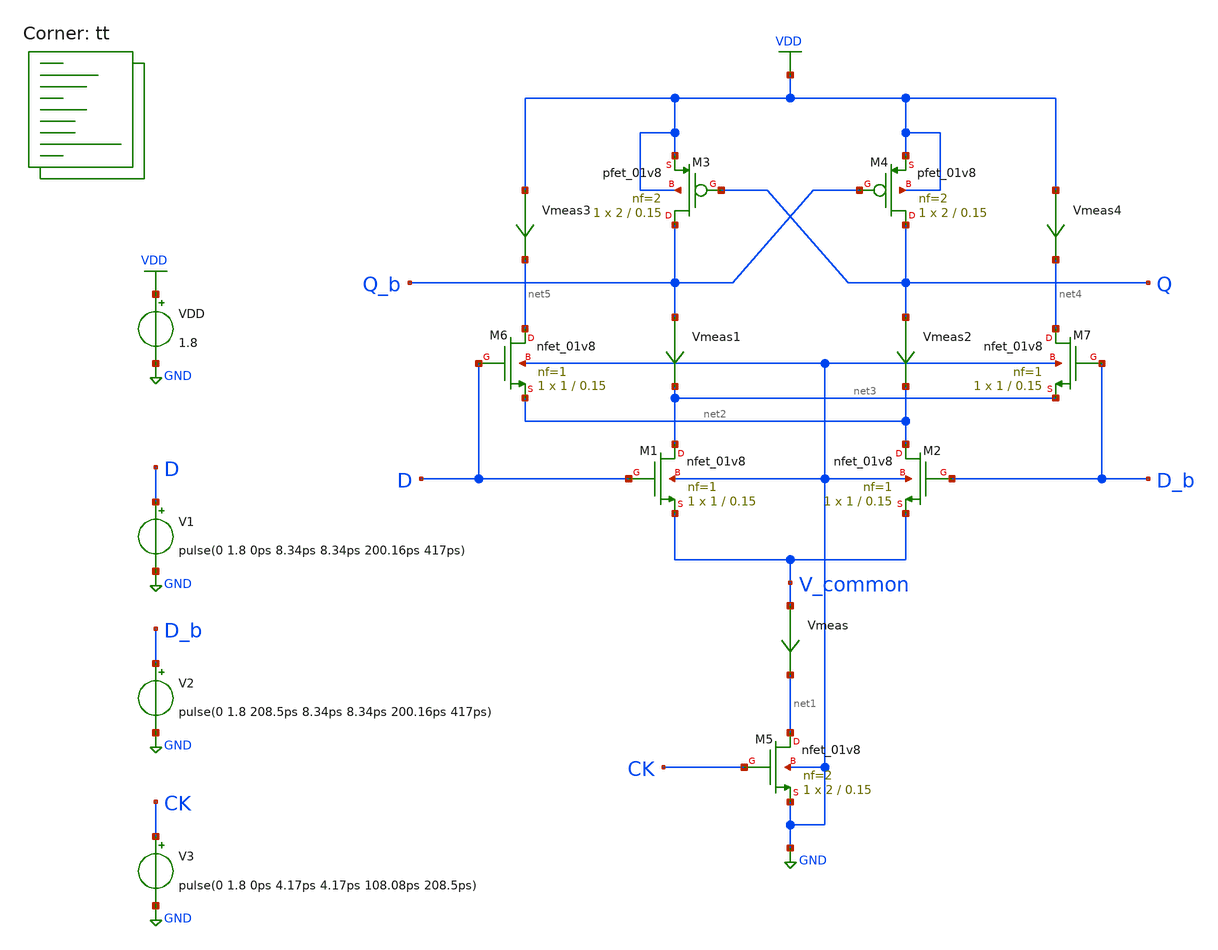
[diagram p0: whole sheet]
** sch_path: projects/pll/divider/xschem_ngspice/tb_xcp_latch_SF2.sch
**.subckt tb_xcp_latch_SF2
VDD VDD GND 1.8
V1 D GND pulse(0 1.8 0ps 8.34ps 8.34ps 200.16ps 417ps)
V2 D_b GND pulse(0 1.8 208.5ps 8.34ps 8.34ps 200.16ps 417ps)
V3 CK GND pulse(0 1.8 0ps 4.17ps 4.17ps 108.08ps 208.5ps)
XM5 net1 CK GND GND sky130_fd_pr__nfet_01v8 L=0.15 W=2 nf=2 ad='int((nf+1)/2) * W/nf * 0.29' as='int((nf+2)/2) * W/nf * 0.29'
+ pd='2*int((nf+1)/2) * (W/nf + 0.29)' ps='2*int((nf+2)/2) * (W/nf + 0.29)' nrd='0.29 / W' nrs='0.29 / W'
+ sa=0 sb=0 sd=0 mult=1 m=1
XM1 net3 D V_common GND sky130_fd_pr__nfet_01v8 L=0.15 W=1 nf=1 ad='int((nf+1)/2) * W/nf * 0.29' as='int((nf+2)/2) * W/nf * 0.29'
+ pd='2*int((nf+1)/2) * (W/nf + 0.29)' ps='2*int((nf+2)/2) * (W/nf + 0.29)' nrd='0.29 / W' nrs='0.29 / W'
+ sa=0 sb=0 sd=0 mult=1 m=1
XM2 net2 D_b V_common GND sky130_fd_pr__nfet_01v8 L=0.15 W=1 nf=1 ad='int((nf+1)/2) * W/nf * 0.29' as='int((nf+2)/2) * W/nf * 0.29'
+ pd='2*int((nf+1)/2) * (W/nf + 0.29)' ps='2*int((nf+2)/2) * (W/nf + 0.29)' nrd='0.29 / W' nrs='0.29 / W'
+ sa=0 sb=0 sd=0 mult=1 m=1
Vmeas V_common net1 0
.save i(vmeas)
Vmeas1 Q_b net3 0
.save i(vmeas1)
Vmeas2 Q net2 0
.save i(vmeas2)
XM3 Q_b Q VDD VDD sky130_fd_pr__pfet_01v8 L=0.15 W=2 nf=2 ad='int((nf+1)/2) * W/nf * 0.29' as='int((nf+2)/2) * W/nf * 0.29'
+ pd='2*int((nf+1)/2) * (W/nf + 0.29)' ps='2*int((nf+2)/2) * (W/nf + 0.29)' nrd='0.29 / W' nrs='0.29 / W'
+ sa=0 sb=0 sd=0 mult=1 m=1
XM4 Q Q_b VDD VDD sky130_fd_pr__pfet_01v8 L=0.15 W=2 nf=2 ad='int((nf+1)/2) * W/nf * 0.29' as='int((nf+2)/2) * W/nf * 0.29'
+ pd='2*int((nf+1)/2) * (W/nf + 0.29)' ps='2*int((nf+2)/2) * (W/nf + 0.29)' nrd='0.29 / W' nrs='0.29 / W'
+ sa=0 sb=0 sd=0 mult=1 m=1
XM6 net5 D net2 GND sky130_fd_pr__nfet_01v8 L=0.15 W=1 nf=1 ad='int((nf+1)/2) * W/nf * 0.29' as='int((nf+2)/2) * W/nf * 0.29'
+ pd='2*int((nf+1)/2) * (W/nf + 0.29)' ps='2*int((nf+2)/2) * (W/nf + 0.29)' nrd='0.29 / W' nrs='0.29 / W'
+ sa=0 sb=0 sd=0 mult=1 m=1
XM7 net4 D_b net3 GND sky130_fd_pr__nfet_01v8 L=0.15 W=1 nf=1 ad='int((nf+1)/2) * W/nf * 0.29' as='int((nf+2)/2) * W/nf * 0.29'
+ pd='2*int((nf+1)/2) * (W/nf + 0.29)' ps='2*int((nf+2)/2) * (W/nf + 0.29)' nrd='0.29 / W' nrs='0.29 / W'
+ sa=0 sb=0 sd=0 mult=1 m=1
Vmeas3 VDD net5 0
.save i(vmeas3)
Vmeas4 VDD net4 0
.save i(vmeas4)
**** begin user architecture code



.include /foss/pdks/sky130A/libs.ref/sky130_fd_sc_hd/spice/sky130_fd_sc_hd.spice

.option method=gear
.option wnflag=1
.option savecurrents

.save @m.xm1.msky130_fd_pr__nfet_01v8[gm] @m.xm1.msky130_fd_pr__nfet_01v8[gm] @m.xm1.msky130_fd_pr__pfet_01v8[gm] @m.xm1.msky130_fd_pr__pfet_01v8[gm] @m.xm1.msky130_fd_pr__nfet_01v8[gm] @m.xm1.msky130_fd_pr__nfet_01v8[gm] @m.xm1.msky130_fd_pr__nfet_01v8[gm] @vmeas @vmeas1 @vmeas2

*.ic v(q_b)=1.8

.control

  save v(d) v(d_b) v(q) v(q_b) v(q1) v(q1_b) v(q2) v(q2_b) v(ck) v(v_common)
  *save all
  *tran 0.1n 1u
  tran 0.2p 5n
  *ac dec 20 1 1T
  remzerovec
  write tb_sr_latch2.raw
  set appendwrite

.endc



.lib $::SKYWATER_MODELS/sky130.lib.spice tt
**** end user architecture code
**.ends
.GLOBAL GND
.GLOBAL VDD
.end
